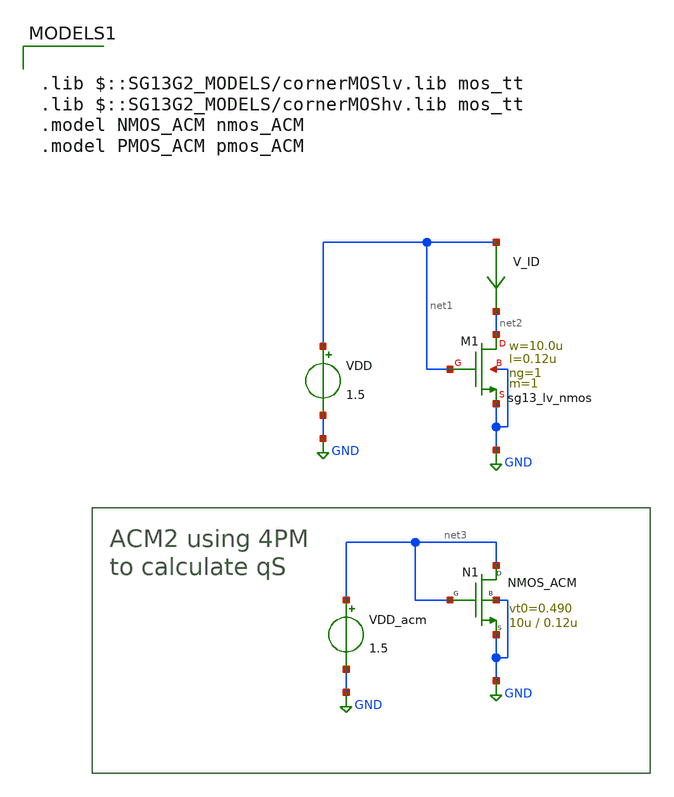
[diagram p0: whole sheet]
** sch_path: legacy/Examples/IHP-SG13/xschem/Extraction/nmos_zeta.sch
**.subckt nmos_zeta
VDD net1 GND 1.5
V_ID net1 net2 0
.save i(v_id)
VDD_acm net3 GND 1.5
XM1 net2 net1 GND GND sg13_lv_nmos w=10.0u l=0.12u ng=1 m=1 mm_ok=1
N1 net3 net3 GND GND NMOS_ACM w=10u l=0.12u n=1.41 is=11.7u vt0=0.490 sigma=52.8m zeta=1p
**** begin user architecture code



.control
pre_osdi /home/gmaranhao/Documents/MOSFET_model/Verilog-A/NMOS_ACM_2V0.osdi
pre_osdi ./psp103_nqs.osdi
save all

op

let IDsat_=i(V_ID)
save IDsat_

let IS=@n1[is]
save IS

let qS=@n1[qS_op]
save qS

let idsat=IDsat_/IS
save idsat

let sqr=sqrt(1+idsat)
save sqr

let aux1 = 2*(qS+1-sqr)
save aux1

let zeta = aux1/idsat
save zeta

set appenwrite
write nmos_zeta.raw


.endc



.lib $::SG13G2_MODELS/cornerMOSlv.lib mos_tt
.lib $::SG13G2_MODELS/cornerMOShv.lib mos_tt
.model NMOS_ACM nmos_ACM
.model PMOS_ACM pmos_ACM

**** end user architecture code
**.ends
.GLOBAL GND
.end
